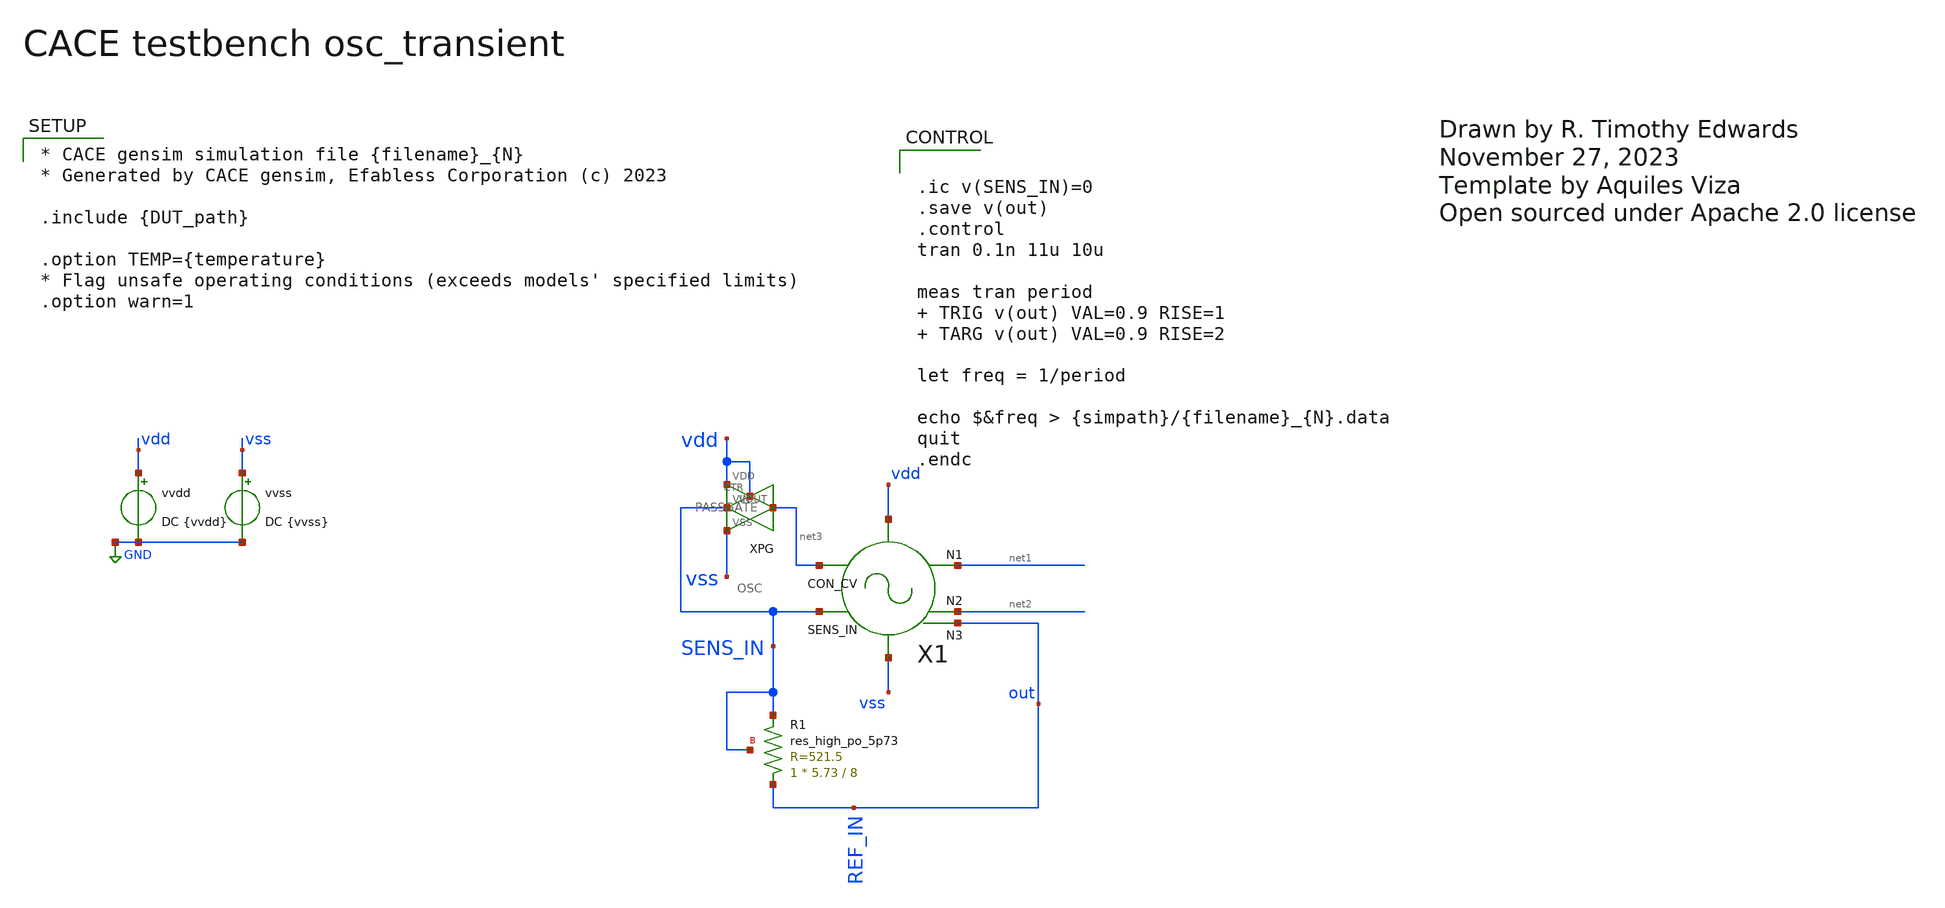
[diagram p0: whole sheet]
** sch_path: modules/OSC/cace/transient.sch
* Open sourced under Apache 2.0 license

* CACE gensim simulation file {filename}_{N}
* Generated by CACE gensim, Efabless Corporation (c) 2023

.include {DUT_path}

.option TEMP={temperature}
* Flag unsafe operating conditions (exceeds models' specified limits)
.option warn=1


**.subckt transient
vvss vss GND DC {vvss}
vvdd vdd GND DC {vvdd}
X1 SENS_IN net1 net2 vdd vss net3 out OSC
XR1 out SENS_IN SENS_IN sky130_fd_pr__res_high_po_5p73 L=8 mult=1 m=1
XPG SENS_IN vdd net3 vdd vss PASSGATE
**** begin user architecture code


.ic v(SENS_IN)=0
.save v(out)
.control
tran 0.1n 11u 10u

meas tran period  TRIG v(out) VAL=0.9 RISE=1  TARG v(out) VAL=0.9 RISE=2

let freq = 1/period

echo $&freq > {simpath}/{filename}_{N}.data
quit
.endc



.lib $env(PDK_ROOT)/$env(PDK)/libs.tech/ngspice/sky130.lib.spice.{corner}.red {corner}

.include $env(PDK_ROOT)/$env(PDK)/libs.ref/sky130_fd_sc_hd/spice/sky130_fd_sc_hd.spice

**** end user architecture code
**.ends
.GLOBAL GND
.end
